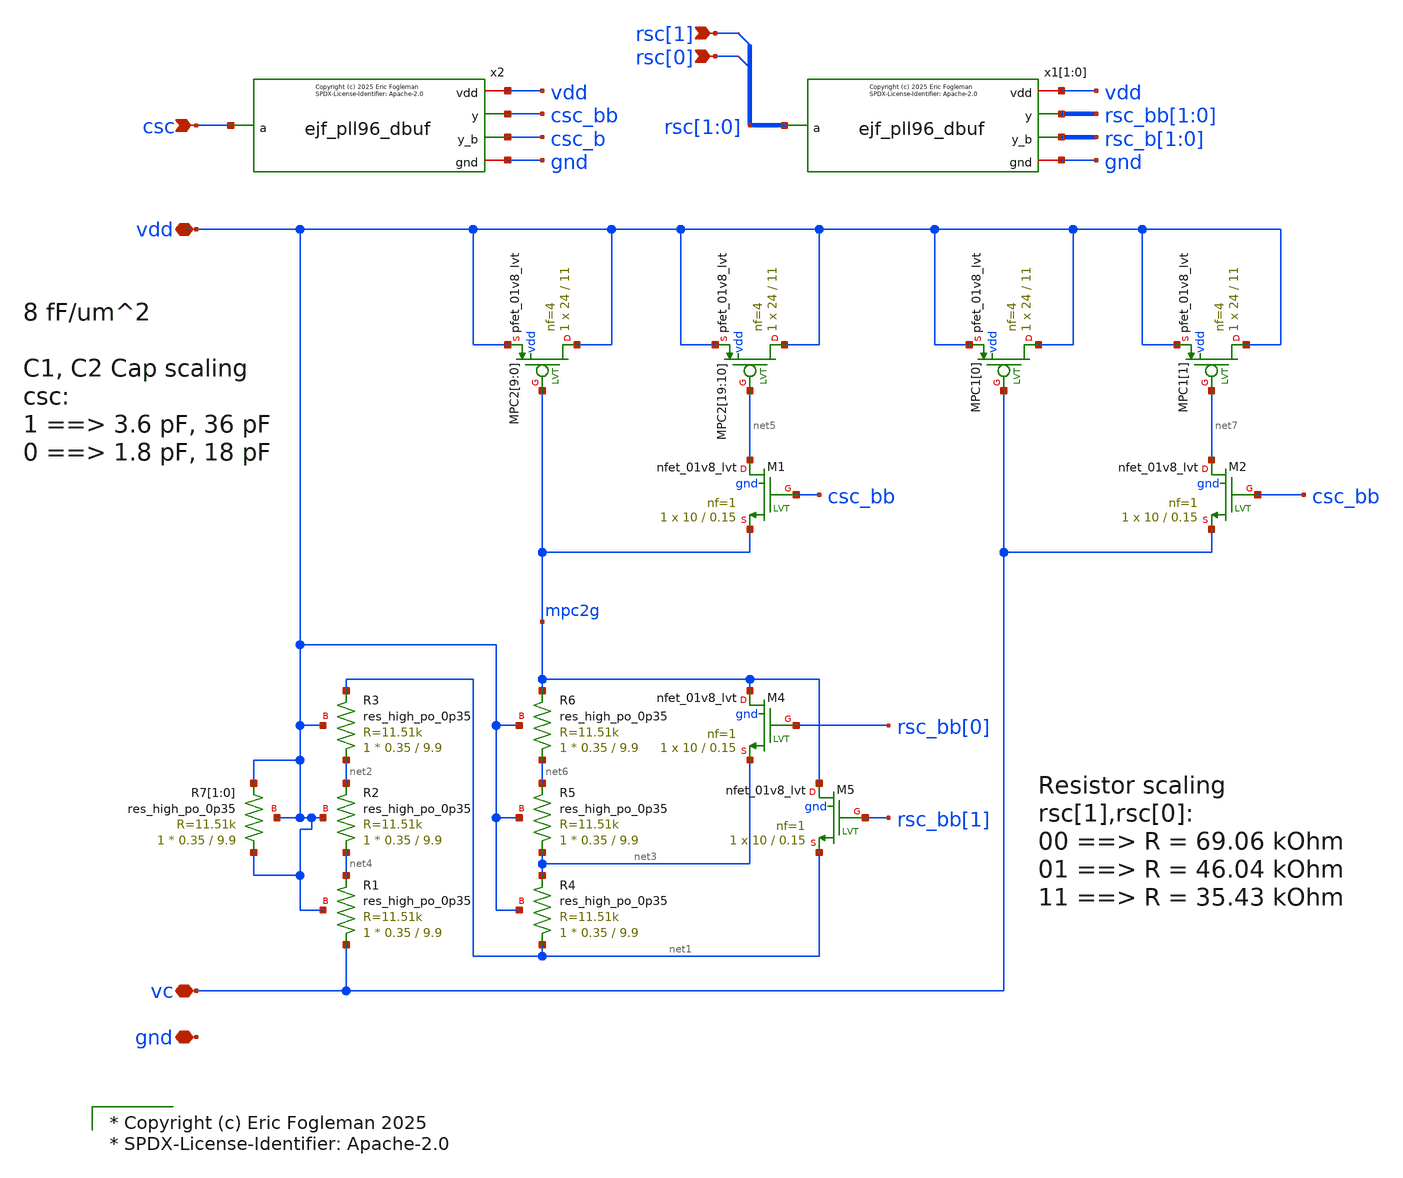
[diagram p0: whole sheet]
** sch_path: xschem/ejf_pll96_lpf.sch
* xschem/ejf_pll96_dbuf.sym:
* Copyright (c) 2025 Eric Fogleman

* Copyright (c) Eric Fogleman 2025
* SPDX-License-Identifier: Apache-2.0

**.subckt ejf_pll96_lpf vc vdd gnd csc rsc[0] rsc[1]
*.iopin vc
*.iopin vdd
*.iopin gnd
*.ipin csc
*.ipin rsc[0]
*.ipin rsc[1]
XMPC2[9] vdd mpc2g vdd vdd sky130_fd_pr__pfet_01v8_lvt L=11 W=24 nf=4 ad='int((nf+1)/2) * W/nf * 0.29'
+ as='int((nf+2)/2) * W/nf * 0.29' pd='2*int((nf+1)/2) * (W/nf + 0.29)' ps='2*int((nf+2)/2) * (W/nf + 0.29)'
+ nrd='0.29 / W' nrs='0.29 / W' sa=0 sb=0 sd=0 mult=1 m=1
XMPC2[8] vdd mpc2g vdd vdd sky130_fd_pr__pfet_01v8_lvt L=11 W=24 nf=4 ad='int((nf+1)/2) * W/nf * 0.29'
+ as='int((nf+2)/2) * W/nf * 0.29' pd='2*int((nf+1)/2) * (W/nf + 0.29)' ps='2*int((nf+2)/2) * (W/nf + 0.29)'
+ nrd='0.29 / W' nrs='0.29 / W' sa=0 sb=0 sd=0 mult=1 m=1
XMPC2[7] vdd mpc2g vdd vdd sky130_fd_pr__pfet_01v8_lvt L=11 W=24 nf=4 ad='int((nf+1)/2) * W/nf * 0.29'
+ as='int((nf+2)/2) * W/nf * 0.29' pd='2*int((nf+1)/2) * (W/nf + 0.29)' ps='2*int((nf+2)/2) * (W/nf + 0.29)'
+ nrd='0.29 / W' nrs='0.29 / W' sa=0 sb=0 sd=0 mult=1 m=1
XMPC2[6] vdd mpc2g vdd vdd sky130_fd_pr__pfet_01v8_lvt L=11 W=24 nf=4 ad='int((nf+1)/2) * W/nf * 0.29'
+ as='int((nf+2)/2) * W/nf * 0.29' pd='2*int((nf+1)/2) * (W/nf + 0.29)' ps='2*int((nf+2)/2) * (W/nf + 0.29)'
+ nrd='0.29 / W' nrs='0.29 / W' sa=0 sb=0 sd=0 mult=1 m=1
XMPC2[5] vdd mpc2g vdd vdd sky130_fd_pr__pfet_01v8_lvt L=11 W=24 nf=4 ad='int((nf+1)/2) * W/nf * 0.29'
+ as='int((nf+2)/2) * W/nf * 0.29' pd='2*int((nf+1)/2) * (W/nf + 0.29)' ps='2*int((nf+2)/2) * (W/nf + 0.29)'
+ nrd='0.29 / W' nrs='0.29 / W' sa=0 sb=0 sd=0 mult=1 m=1
XMPC2[4] vdd mpc2g vdd vdd sky130_fd_pr__pfet_01v8_lvt L=11 W=24 nf=4 ad='int((nf+1)/2) * W/nf * 0.29'
+ as='int((nf+2)/2) * W/nf * 0.29' pd='2*int((nf+1)/2) * (W/nf + 0.29)' ps='2*int((nf+2)/2) * (W/nf + 0.29)'
+ nrd='0.29 / W' nrs='0.29 / W' sa=0 sb=0 sd=0 mult=1 m=1
XMPC2[3] vdd mpc2g vdd vdd sky130_fd_pr__pfet_01v8_lvt L=11 W=24 nf=4 ad='int((nf+1)/2) * W/nf * 0.29'
+ as='int((nf+2)/2) * W/nf * 0.29' pd='2*int((nf+1)/2) * (W/nf + 0.29)' ps='2*int((nf+2)/2) * (W/nf + 0.29)'
+ nrd='0.29 / W' nrs='0.29 / W' sa=0 sb=0 sd=0 mult=1 m=1
XMPC2[2] vdd mpc2g vdd vdd sky130_fd_pr__pfet_01v8_lvt L=11 W=24 nf=4 ad='int((nf+1)/2) * W/nf * 0.29'
+ as='int((nf+2)/2) * W/nf * 0.29' pd='2*int((nf+1)/2) * (W/nf + 0.29)' ps='2*int((nf+2)/2) * (W/nf + 0.29)'
+ nrd='0.29 / W' nrs='0.29 / W' sa=0 sb=0 sd=0 mult=1 m=1
XMPC2[1] vdd mpc2g vdd vdd sky130_fd_pr__pfet_01v8_lvt L=11 W=24 nf=4 ad='int((nf+1)/2) * W/nf * 0.29'
+ as='int((nf+2)/2) * W/nf * 0.29' pd='2*int((nf+1)/2) * (W/nf + 0.29)' ps='2*int((nf+2)/2) * (W/nf + 0.29)'
+ nrd='0.29 / W' nrs='0.29 / W' sa=0 sb=0 sd=0 mult=1 m=1
XMPC2[0] vdd mpc2g vdd vdd sky130_fd_pr__pfet_01v8_lvt L=11 W=24 nf=4 ad='int((nf+1)/2) * W/nf * 0.29'
+ as='int((nf+2)/2) * W/nf * 0.29' pd='2*int((nf+1)/2) * (W/nf + 0.29)' ps='2*int((nf+2)/2) * (W/nf + 0.29)'
+ nrd='0.29 / W' nrs='0.29 / W' sa=0 sb=0 sd=0 mult=1 m=1
XMPC1[0] vdd vc vdd vdd sky130_fd_pr__pfet_01v8_lvt L=11 W=24 nf=4 ad='int((nf+1)/2) * W/nf * 0.29' as='int((nf+2)/2) * W/nf * 0.29'
+ pd='2*int((nf+1)/2) * (W/nf + 0.29)' ps='2*int((nf+2)/2) * (W/nf + 0.29)' nrd='0.29 / W' nrs='0.29 / W'
+ sa=0 sb=0 sd=0 mult=1 m=1
XMPC2[19] vdd net5 vdd vdd sky130_fd_pr__pfet_01v8_lvt L=11 W=24 nf=4 ad='int((nf+1)/2) * W/nf * 0.29'
+ as='int((nf+2)/2) * W/nf * 0.29' pd='2*int((nf+1)/2) * (W/nf + 0.29)' ps='2*int((nf+2)/2) * (W/nf + 0.29)'
+ nrd='0.29 / W' nrs='0.29 / W' sa=0 sb=0 sd=0 mult=1 m=1
XMPC2[18] vdd net5 vdd vdd sky130_fd_pr__pfet_01v8_lvt L=11 W=24 nf=4 ad='int((nf+1)/2) * W/nf * 0.29'
+ as='int((nf+2)/2) * W/nf * 0.29' pd='2*int((nf+1)/2) * (W/nf + 0.29)' ps='2*int((nf+2)/2) * (W/nf + 0.29)'
+ nrd='0.29 / W' nrs='0.29 / W' sa=0 sb=0 sd=0 mult=1 m=1
XMPC2[17] vdd net5 vdd vdd sky130_fd_pr__pfet_01v8_lvt L=11 W=24 nf=4 ad='int((nf+1)/2) * W/nf * 0.29'
+ as='int((nf+2)/2) * W/nf * 0.29' pd='2*int((nf+1)/2) * (W/nf + 0.29)' ps='2*int((nf+2)/2) * (W/nf + 0.29)'
+ nrd='0.29 / W' nrs='0.29 / W' sa=0 sb=0 sd=0 mult=1 m=1
XMPC2[16] vdd net5 vdd vdd sky130_fd_pr__pfet_01v8_lvt L=11 W=24 nf=4 ad='int((nf+1)/2) * W/nf * 0.29'
+ as='int((nf+2)/2) * W/nf * 0.29' pd='2*int((nf+1)/2) * (W/nf + 0.29)' ps='2*int((nf+2)/2) * (W/nf + 0.29)'
+ nrd='0.29 / W' nrs='0.29 / W' sa=0 sb=0 sd=0 mult=1 m=1
XMPC2[15] vdd net5 vdd vdd sky130_fd_pr__pfet_01v8_lvt L=11 W=24 nf=4 ad='int((nf+1)/2) * W/nf * 0.29'
+ as='int((nf+2)/2) * W/nf * 0.29' pd='2*int((nf+1)/2) * (W/nf + 0.29)' ps='2*int((nf+2)/2) * (W/nf + 0.29)'
+ nrd='0.29 / W' nrs='0.29 / W' sa=0 sb=0 sd=0 mult=1 m=1
XMPC2[14] vdd net5 vdd vdd sky130_fd_pr__pfet_01v8_lvt L=11 W=24 nf=4 ad='int((nf+1)/2) * W/nf * 0.29'
+ as='int((nf+2)/2) * W/nf * 0.29' pd='2*int((nf+1)/2) * (W/nf + 0.29)' ps='2*int((nf+2)/2) * (W/nf + 0.29)'
+ nrd='0.29 / W' nrs='0.29 / W' sa=0 sb=0 sd=0 mult=1 m=1
XMPC2[13] vdd net5 vdd vdd sky130_fd_pr__pfet_01v8_lvt L=11 W=24 nf=4 ad='int((nf+1)/2) * W/nf * 0.29'
+ as='int((nf+2)/2) * W/nf * 0.29' pd='2*int((nf+1)/2) * (W/nf + 0.29)' ps='2*int((nf+2)/2) * (W/nf + 0.29)'
+ nrd='0.29 / W' nrs='0.29 / W' sa=0 sb=0 sd=0 mult=1 m=1
XMPC2[12] vdd net5 vdd vdd sky130_fd_pr__pfet_01v8_lvt L=11 W=24 nf=4 ad='int((nf+1)/2) * W/nf * 0.29'
+ as='int((nf+2)/2) * W/nf * 0.29' pd='2*int((nf+1)/2) * (W/nf + 0.29)' ps='2*int((nf+2)/2) * (W/nf + 0.29)'
+ nrd='0.29 / W' nrs='0.29 / W' sa=0 sb=0 sd=0 mult=1 m=1
XMPC2[11] vdd net5 vdd vdd sky130_fd_pr__pfet_01v8_lvt L=11 W=24 nf=4 ad='int((nf+1)/2) * W/nf * 0.29'
+ as='int((nf+2)/2) * W/nf * 0.29' pd='2*int((nf+1)/2) * (W/nf + 0.29)' ps='2*int((nf+2)/2) * (W/nf + 0.29)'
+ nrd='0.29 / W' nrs='0.29 / W' sa=0 sb=0 sd=0 mult=1 m=1
XMPC2[10] vdd net5 vdd vdd sky130_fd_pr__pfet_01v8_lvt L=11 W=24 nf=4 ad='int((nf+1)/2) * W/nf * 0.29'
+ as='int((nf+2)/2) * W/nf * 0.29' pd='2*int((nf+1)/2) * (W/nf + 0.29)' ps='2*int((nf+2)/2) * (W/nf + 0.29)'
+ nrd='0.29 / W' nrs='0.29 / W' sa=0 sb=0 sd=0 mult=1 m=1
XR7[1] vdd vdd vdd sky130_fd_pr__res_high_po_0p35 L=9.9 mult=1 m=1
XR7[0] vdd vdd vdd sky130_fd_pr__res_high_po_0p35 L=9.9 mult=1 m=1
XMPC1[1] vdd net7 vdd vdd sky130_fd_pr__pfet_01v8_lvt L=11 W=24 nf=4 ad='int((nf+1)/2) * W/nf * 0.29'
+ as='int((nf+2)/2) * W/nf * 0.29' pd='2*int((nf+1)/2) * (W/nf + 0.29)' ps='2*int((nf+2)/2) * (W/nf + 0.29)'
+ nrd='0.29 / W' nrs='0.29 / W' sa=0 sb=0 sd=0 mult=1 m=1
x2 vdd csc csc_bb csc_b gnd ejf_pll96_dbuf
XM1 net5 csc_bb mpc2g gnd sky130_fd_pr__nfet_01v8_lvt L=0.15 W=10 nf=1 ad='int((nf+1)/2) * W/nf * 0.29'
+ as='int((nf+2)/2) * W/nf * 0.29' pd='2*int((nf+1)/2) * (W/nf + 0.29)' ps='2*int((nf+2)/2) * (W/nf + 0.29)'
+ nrd='0.29 / W' nrs='0.29 / W' sa=0 sb=0 sd=0 mult=1 m=1
XM2 net7 csc_bb vc gnd sky130_fd_pr__nfet_01v8_lvt L=0.15 W=10 nf=1 ad='int((nf+1)/2) * W/nf * 0.29'
+ as='int((nf+2)/2) * W/nf * 0.29' pd='2*int((nf+1)/2) * (W/nf + 0.29)' ps='2*int((nf+2)/2) * (W/nf + 0.29)'
+ nrd='0.29 / W' nrs='0.29 / W' sa=0 sb=0 sd=0 mult=1 m=1
XR1 vc net4 vdd sky130_fd_pr__res_high_po_0p35 L=9.9 mult=1 m=1
XR2 net4 net2 vdd sky130_fd_pr__res_high_po_0p35 L=9.9 mult=1 m=1
XR3 net2 net1 vdd sky130_fd_pr__res_high_po_0p35 L=9.9 mult=1 m=1
XR4 net1 net3 vdd sky130_fd_pr__res_high_po_0p35 L=9.9 mult=1 m=1
XR5 net3 net6 vdd sky130_fd_pr__res_high_po_0p35 L=9.9 mult=1 m=1
XR6 net6 mpc2g vdd sky130_fd_pr__res_high_po_0p35 L=9.9 mult=1 m=1
XM4 mpc2g rsc_bb[0] net3 gnd sky130_fd_pr__nfet_01v8_lvt L=0.15 W=10 nf=1 ad='int((nf+1)/2) * W/nf * 0.29'
+ as='int((nf+2)/2) * W/nf * 0.29' pd='2*int((nf+1)/2) * (W/nf + 0.29)' ps='2*int((nf+2)/2) * (W/nf + 0.29)'
+ nrd='0.29 / W' nrs='0.29 / W' sa=0 sb=0 sd=0 mult=1 m=1
XM5 mpc2g rsc_bb[1] net1 gnd sky130_fd_pr__nfet_01v8_lvt L=0.15 W=10 nf=1 ad='int((nf+1)/2) * W/nf * 0.29'
+ as='int((nf+2)/2) * W/nf * 0.29' pd='2*int((nf+1)/2) * (W/nf + 0.29)' ps='2*int((nf+2)/2) * (W/nf + 0.29)'
+ nrd='0.29 / W' nrs='0.29 / W' sa=0 sb=0 sd=0 mult=1 m=1
x1[1] vdd rsc[1] rsc_bb[1] rsc_b[1] gnd ejf_pll96_dbuf
x1[0] vdd rsc[0] rsc_bb[0] rsc_b[0] gnd ejf_pll96_dbuf
**.ends

* expanding   symbol:  ejf_pll96_dbuf.sym # of pins=5
** sym_path: xschem/ejf_pll96_dbuf.sym
** sch_path: xschem/ejf_pll96_dbuf.sch
.subckt ejf_pll96_dbuf vdd a y y_b gnd
*.ipin a
*.iopin vdd
*.iopin gnd
*.opin y
*.opin y_b
XMP1 y_b a vdd vdd sky130_fd_pr__pfet_01v8_hvt L=0.15 W=2 nf=1 ad='int((nf+1)/2) * W/nf * 0.29' as='int((nf+2)/2) * W/nf * 0.29'
+ pd='2*int((nf+1)/2) * (W/nf + 0.29)' ps='2*int((nf+2)/2) * (W/nf + 0.29)' nrd='0.29 / W' nrs='0.29 / W'
+ sa=0 sb=0 sd=0 mult=1 m=1
XMP3 y y_b vdd vdd sky130_fd_pr__pfet_01v8_hvt L=0.15 W=2 nf=1 ad='int((nf+1)/2) * W/nf * 0.29' as='int((nf+2)/2) * W/nf * 0.29'
+ pd='2*int((nf+1)/2) * (W/nf + 0.29)' ps='2*int((nf+2)/2) * (W/nf + 0.29)' nrd='0.29 / W' nrs='0.29 / W'
+ sa=0 sb=0 sd=0 mult=1 m=1
XMN4 y y_b gnd gnd sky130_fd_pr__nfet_01v8 L=0.15 W=1 nf=1 ad='int((nf+1)/2) * W/nf * 0.29' as='int((nf+2)/2) * W/nf * 0.29'
+ pd='2*int((nf+1)/2) * (W/nf + 0.29)' ps='2*int((nf+2)/2) * (W/nf + 0.29)' nrd='0.29 / W' nrs='0.29 / W'
+ sa=0 sb=0 sd=0 mult=1 m=1
XMN2 y_b a gnd gnd sky130_fd_pr__nfet_01v8 L=0.15 W=1 nf=1 ad='int((nf+1)/2) * W/nf * 0.29' as='int((nf+2)/2) * W/nf * 0.29'
+ pd='2*int((nf+1)/2) * (W/nf + 0.29)' ps='2*int((nf+2)/2) * (W/nf + 0.29)' nrd='0.29 / W' nrs='0.29 / W'
+ sa=0 sb=0 sd=0 mult=1 m=1
**** begin user architecture code

* Copyright (c) Eric Fogleman 2025
* SPDX-License-Identifier: Apache-2.0

**** end user architecture code
.ends

.end
